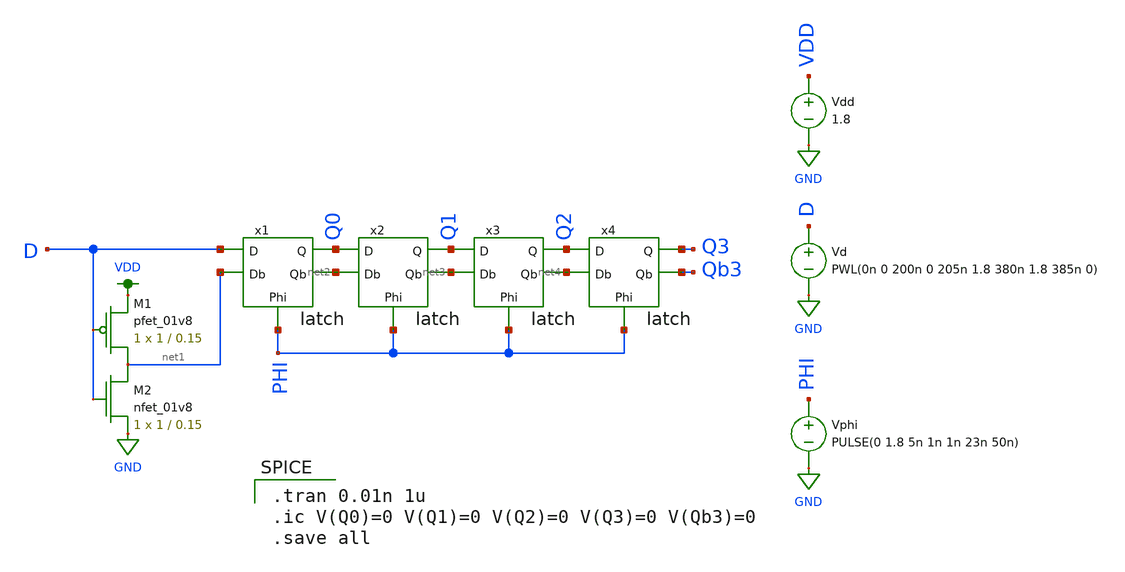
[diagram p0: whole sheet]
** sch_path: mp2/sr_testharness.sch
**.subckt sr_testharness
x1 D Q0 net1 net2 PHI latch
x2 Q0 Q1 net2 net3 PHI latch
x3 Q1 Q2 net3 net4 PHI latch
x4 Q2 Q3 net4 Qb3 PHI latch
XM1 net1 D VDD VDD sky130_fd_pr__pfet_01v8 L=0.15 W=1 nf=1 ad='int((nf+1)/2) * W/nf * 0.29' as='int((nf+2)/2) * W/nf * 0.29'
+ pd='2*int((nf+1)/2) * (W/nf + 0.29)' ps='2*int((nf+2)/2) * (W/nf + 0.29)' nrd='0.29 / W' nrs='0.29 / W'
+ sa=0 sb=0 sd=0 mult=1 m=1
XM2 net1 D GND GND sky130_fd_pr__nfet_01v8 L=0.15 W=1 nf=1 ad='int((nf+1)/2) * W/nf * 0.29' as='int((nf+2)/2) * W/nf * 0.29'
+ pd='2*int((nf+1)/2) * (W/nf + 0.29)' ps='2*int((nf+2)/2) * (W/nf + 0.29)' nrd='0.29 / W' nrs='0.29 / W'
+ sa=0 sb=0 sd=0 mult=1 m=1
Vd D GND PWL(0n 0 200n 0 205n 1.8 380n 1.8 385n 0)
Vphi PHI GND PULSE(0 1.8 5n 1n 1n 23n 50n)
Vdd VDD GND 1.8
**** begin user architecture code

.tran 0.01n 1u
.ic V(Q0)=0 V(Q1)=0 V(Q2)=0 V(Q3)=0 V(Qb3)=0
.save all


.option wnflag=1
.lib ~/skywater/skywater-pdk/libraries/sky130_fd_pr_ngspice/latest/models/sky130.lib.spice tt

**** end user architecture code
**.ends

* expanding   symbol:  /home/madvlsi/Documents/mp2/latch.sym # of pins=5
** sym_path: mp2/latch.sym
** sch_path: mp2/latch.sch
.subckt latch D Q Db Qb Phi
*.ipin D
*.ipin Db
*.opin Q
*.opin Qb
*.ipin Phi
XM1 net1 net2 VDD VDD sky130_fd_pr__pfet_01v8 L=0.15 W=1 nf=1 ad='int((nf+1)/2) * W/nf * 0.29' as='int((nf+2)/2) * W/nf * 0.29'
+ pd='2*int((nf+1)/2) * (W/nf + 0.29)' ps='2*int((nf+2)/2) * (W/nf + 0.29)' nrd='0.29 / W' nrs='0.29 / W'
+ sa=0 sb=0 sd=0 mult=1 m=1
XM2 net2 net1 VDD VDD sky130_fd_pr__pfet_01v8 L=0.15 W=1 nf=1 ad='int((nf+1)/2) * W/nf * 0.29' as='int((nf+2)/2) * W/nf * 0.29'
+ pd='2*int((nf+1)/2) * (W/nf + 0.29)' ps='2*int((nf+2)/2) * (W/nf + 0.29)' nrd='0.29 / W' nrs='0.29 / W'
+ sa=0 sb=0 sd=0 mult=1 m=1
XM3 net3 net2 net1 GND sky130_fd_pr__nfet_01v8 L=0.15 W=1 nf=1 ad='int((nf+1)/2) * W/nf * 0.29' as='int((nf+2)/2) * W/nf * 0.29'
+ pd='2*int((nf+1)/2) * (W/nf + 0.29)' ps='2*int((nf+2)/2) * (W/nf + 0.29)' nrd='0.29 / W' nrs='0.29 / W'
+ sa=0 sb=0 sd=0 mult=1 m=1
XM4 net3 net1 net2 GND sky130_fd_pr__nfet_01v8 L=0.15 W=1 nf=1 ad='int((nf+1)/2) * W/nf * 0.29' as='int((nf+2)/2) * W/nf * 0.29'
+ pd='2*int((nf+1)/2) * (W/nf + 0.29)' ps='2*int((nf+2)/2) * (W/nf + 0.29)' nrd='0.29 / W' nrs='0.29 / W'
+ sa=0 sb=0 sd=0 mult=1 m=1
XM5 net3 Phi GND GND sky130_fd_pr__nfet_01v8 L=0.15 W=4.01 nf=1 ad='int((nf+1)/2) * W/nf * 0.29' as='int((nf+2)/2) * W/nf * 0.29'
+ pd='2*int((nf+1)/2) * (W/nf + 0.29)' ps='2*int((nf+2)/2) * (W/nf + 0.29)' nrd='0.29 / W' nrs='0.29 / W'
+ sa=0 sb=0 sd=0 mult=1 m=1
XM6 net1 Phi Db VDD sky130_fd_pr__pfet_01v8 L=0.15 W=1 nf=1 ad='int((nf+1)/2) * W/nf * 0.29' as='int((nf+2)/2) * W/nf * 0.29'
+ pd='2*int((nf+1)/2) * (W/nf + 0.29)' ps='2*int((nf+2)/2) * (W/nf + 0.29)' nrd='0.29 / W' nrs='0.29 / W'
+ sa=0 sb=0 sd=0 mult=1 m=1
XM7 net2 Phi D VDD sky130_fd_pr__pfet_01v8 L=0.15 W=1 nf=1 ad='int((nf+1)/2) * W/nf * 0.29' as='int((nf+2)/2) * W/nf * 0.29'
+ pd='2*int((nf+1)/2) * (W/nf + 0.29)' ps='2*int((nf+2)/2) * (W/nf + 0.29)' nrd='0.29 / W' nrs='0.29 / W'
+ sa=0 sb=0 sd=0 mult=1 m=1
XM8 Qb Q net4 VDD sky130_fd_pr__pfet_01v8 L=0.15 W=1 nf=1 ad='int((nf+1)/2) * W/nf * 0.29' as='int((nf+2)/2) * W/nf * 0.29'
+ pd='2*int((nf+1)/2) * (W/nf + 0.29)' ps='2*int((nf+2)/2) * (W/nf + 0.29)' nrd='0.29 / W' nrs='0.29 / W'
+ sa=0 sb=0 sd=0 mult=1 m=1
XM9 Q Qb net4 VDD sky130_fd_pr__pfet_01v8 L=0.15 W=1 nf=1 ad='int((nf+1)/2) * W/nf * 0.29' as='int((nf+2)/2) * W/nf * 0.29'
+ pd='2*int((nf+1)/2) * (W/nf + 0.29)' ps='2*int((nf+2)/2) * (W/nf + 0.29)' nrd='0.29 / W' nrs='0.29 / W'
+ sa=0 sb=0 sd=0 mult=1 m=1
XM10 Qb Q GND GND sky130_fd_pr__nfet_01v8 L=0.15 W=1 nf=1 ad='int((nf+1)/2) * W/nf * 0.29' as='int((nf+2)/2) * W/nf * 0.29'
+ pd='2*int((nf+1)/2) * (W/nf + 0.29)' ps='2*int((nf+2)/2) * (W/nf + 0.29)' nrd='0.29 / W' nrs='0.29 / W'
+ sa=0 sb=0 sd=0 mult=1 m=1
XM11 Q Qb GND GND sky130_fd_pr__nfet_01v8 L=0.15 W=1 nf=1 ad='int((nf+1)/2) * W/nf * 0.29' as='int((nf+2)/2) * W/nf * 0.29'
+ pd='2*int((nf+1)/2) * (W/nf + 0.29)' ps='2*int((nf+2)/2) * (W/nf + 0.29)' nrd='0.29 / W' nrs='0.29 / W'
+ sa=0 sb=0 sd=0 mult=1 m=1
XM12 Qb Phi net1 GND sky130_fd_pr__nfet_01v8 L=0.15 W=1 nf=1 ad='int((nf+1)/2) * W/nf * 0.29' as='int((nf+2)/2) * W/nf * 0.29'
+ pd='2*int((nf+1)/2) * (W/nf + 0.29)' ps='2*int((nf+2)/2) * (W/nf + 0.29)' nrd='0.29 / W' nrs='0.29 / W'
+ sa=0 sb=0 sd=0 mult=1 m=1
XM13 Q Phi net2 GND sky130_fd_pr__nfet_01v8 L=0.15 W=1 nf=1 ad='int((nf+1)/2) * W/nf * 0.29' as='int((nf+2)/2) * W/nf * 0.29'
+ pd='2*int((nf+1)/2) * (W/nf + 0.29)' ps='2*int((nf+2)/2) * (W/nf + 0.29)' nrd='0.29 / W' nrs='0.29 / W'
+ sa=0 sb=0 sd=0 mult=1 m=1
XM14 net4 Phi VDD VDD sky130_fd_pr__pfet_01v8 L=0.15 W=4.01 nf=1 ad='int((nf+1)/2) * W/nf * 0.29' as='int((nf+2)/2) * W/nf * 0.29'
+ pd='2*int((nf+1)/2) * (W/nf + 0.29)' ps='2*int((nf+2)/2) * (W/nf + 0.29)' nrd='0.29 / W' nrs='0.29 / W'
+ sa=0 sb=0 sd=0 mult=1 m=1
.ends

.GLOBAL VDD
.GLOBAL GND
.end
